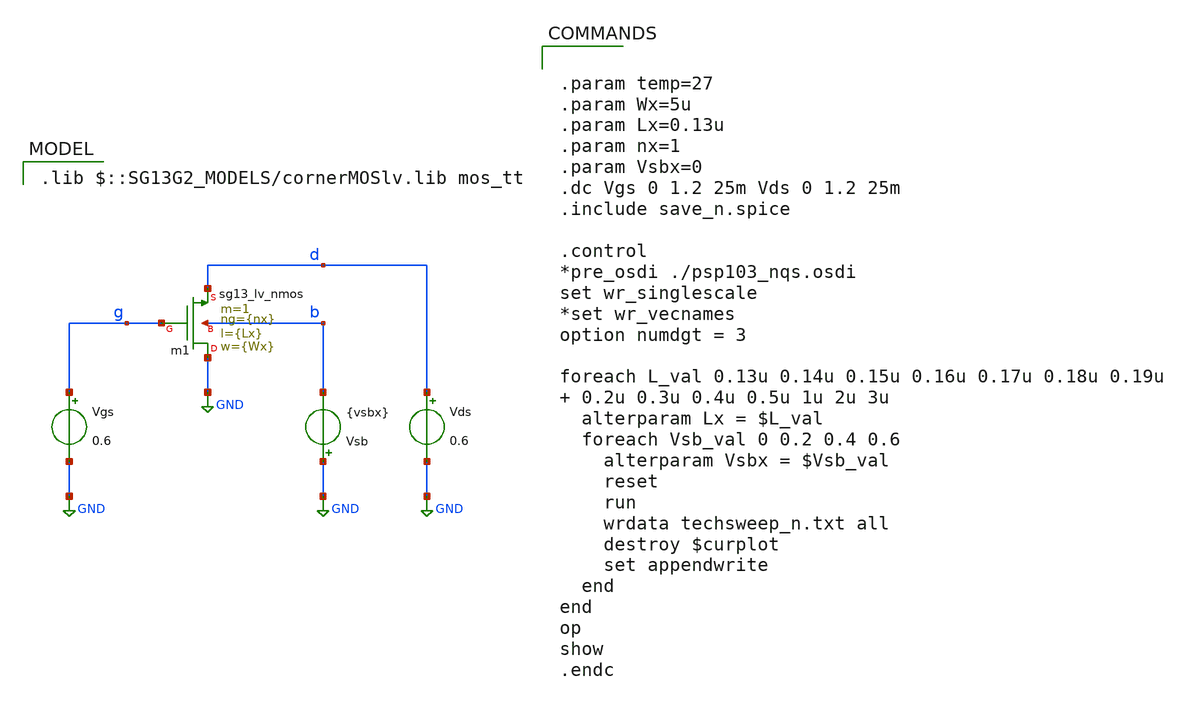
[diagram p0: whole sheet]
** sch_path: 02_gm_id/src/techsweep_n.sch
**.subckt techsweep_n
Xm1 GND g d b sg13_lv_nmos w={Wx} l={Lx} ng={nx} m=1 mm_ok=1
Vgs g GND 0.6
Vds d GND 0.6
Vsb GND b {vsbx}
**** begin user architecture code
 .lib $::SG13G2_MODELS/cornerMOSlv.lib mos_tt



.param temp=27
.param Wx=5u
.param Lx=0.13u
.param nx=1
.param Vsbx=0
.dc Vgs 0 1.2 25m Vds 0 1.2 25m
.include save_n.spice

.control
*pre_osdi ./psp103_nqs.osdi
set wr_singlescale
*set wr_vecnames
option numdgt = 3

foreach L_val 0.13u 0.14u 0.15u 0.16u 0.17u 0.18u 0.19u  0.2u 0.3u 0.4u 0.5u 1u 2u 3u
  alterparam Lx = $L_val
  foreach Vsb_val 0 0.2 0.4 0.6
    alterparam Vsbx = $Vsb_val
    reset
    run
    wrdata techsweep_n.txt all
    destroy $curplot
    set appendwrite
  end
end
op
show
.endc


**** end user architecture code
**.ends
.GLOBAL GND
.end
